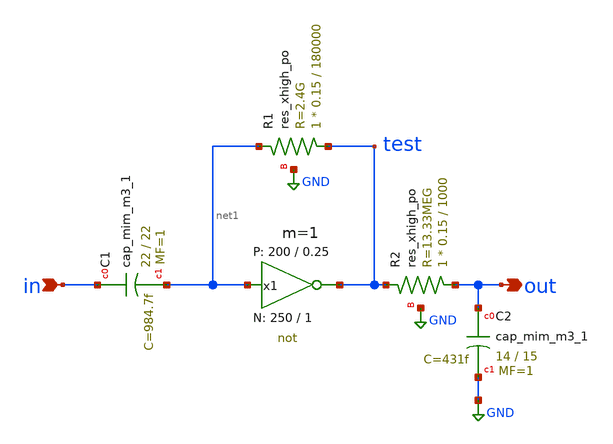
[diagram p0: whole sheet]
** sch_path: Amplifier_Inv/xschem/inv_sky130_a_v1.sch
* StefanSchippers/xschem_sky130/sky130_tests/not.sch:
* Copyright 2021 Stefan Frederik Schippers
* Licensed under the Apache License, Version 2.0 (the "License");
**.subckt inv_sky130_a_v1 in out
*.ipin in
*.opin out
x1 test net1 VCC VSS not W_N=250 L_N=1 W_P=200 L_P=0.25 m=1
XC2 out GND sky130_fd_pr__cap_mim_m3_1 W=14 L=15 MF=1 m=1
XR1 test net1 GND sky130_fd_pr__res_xhigh_po W=0.15 L=180000 mult=1 m=1
XR2 out test GND sky130_fd_pr__res_xhigh_po W=0.15 L=1000 mult=1 m=1
XC1 in net1 sky130_fd_pr__cap_mim_m3_1 W=22 L=22 MF=1 m=1
**.ends

* expanding   symbol:  sky130_tests/not.sym # of pins=2
** sym_path: sky130_tests/not.sym
** sch_path: sky130_tests/not.sch
.subckt not y a VCCPIN VSSPIN     W_N=1 L_N=0.15 W_P=2 L_P=0.15
*.opin y
*.ipin a
XM1 DN a VSSPIN VSSPIN sky130_fd_pr__nfet_01v8 L=L_N W=W_N nf=1 ad='int((1 + 1)/2) * W_N / 1 * 0.29'
+ as='int((1 + 2)/2) * W_N / 1 * 0.29' pd='2*int((1 + 1)/2) * (W_N / 1 + 0.29)' ps='2*int((1 + 2)/2) * (W_N / 1 + 0.29)'
+ nrd='0.29 / W_N ' nrs='0.29 / W_N ' sa=0 sb=0 sd=0 mult=1 m=1
XM2 DP a VCCPIN VCCPIN sky130_fd_pr__pfet_01v8 L=L_P W=W_P nf=1 ad='int((nf+1)/2) * W/nf * 0.29' as='int((nf+2)/2) * W/nf * 0.29'
+ pd='2*int((nf+1)/2) * (W/nf + 0.29)' ps='2*int((nf+2)/2) * (W/nf + 0.29)' nrd='0.29 / W' nrs='0.29 / W'
+ sa=0 sb=0 sd=0 mult=1 m=1
Vmeas DP y 0
.save i(vmeas)
Vmeas1 y DN 0
.save i(vmeas1)
.save v(dp)
.save v(dn)
.ends

.GLOBAL GND
.end
